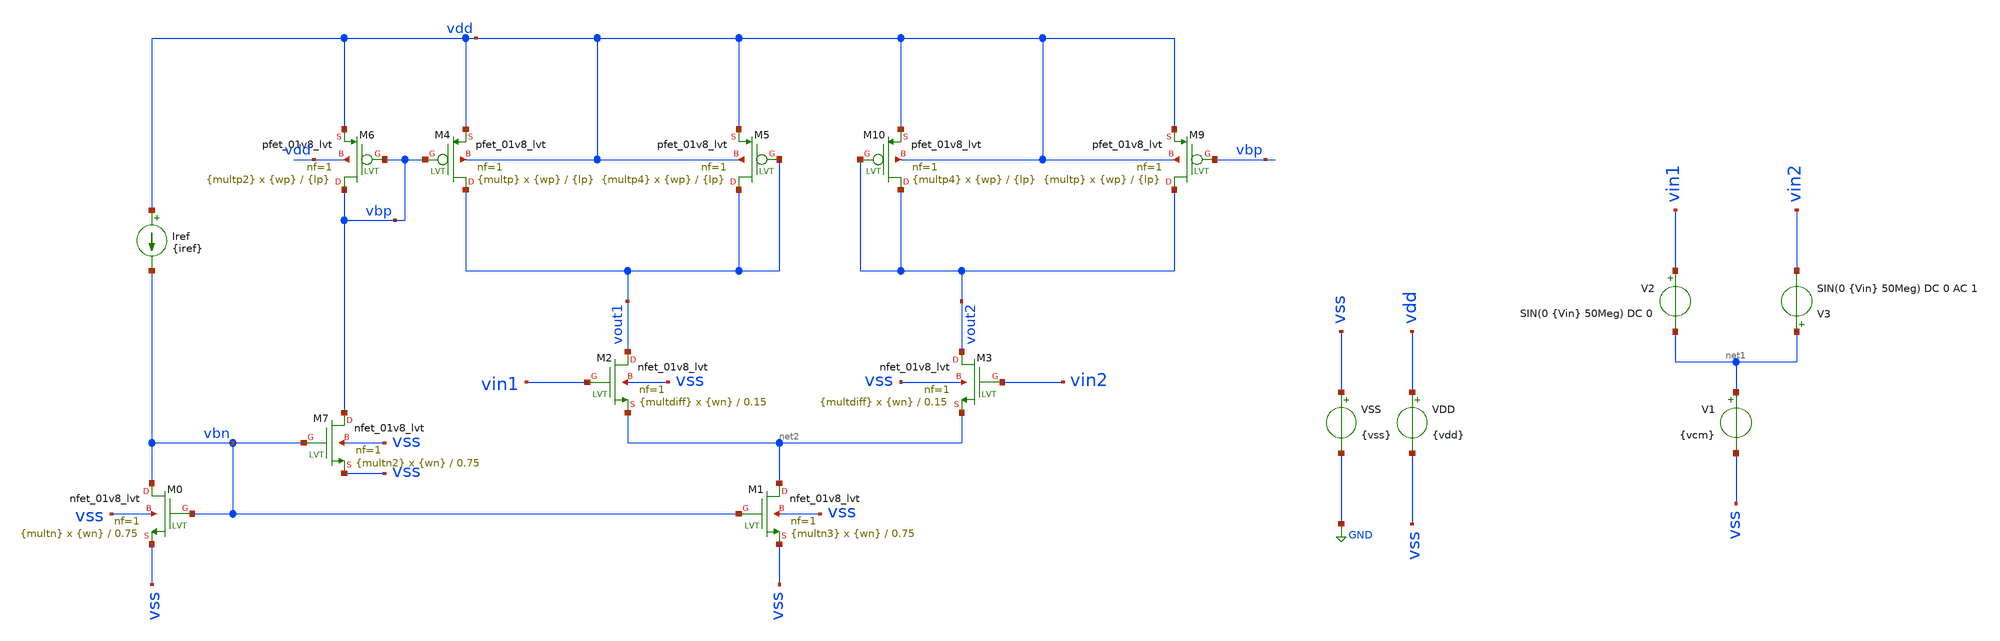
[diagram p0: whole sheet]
** sch_path: tp3/tp3_2.sch
**.subckt tp3_2
Iref vdd vbn {iref}
VSS vss GND {vss}
VDD vdd vss {vdd}
V1 net1 vss {vcm}
XM1 net2 vbn vss vss sky130_fd_pr__nfet_01v8_lvt L=0.75 W={wn} nf=1 ad='int((nf+1)/2) * W/nf * 0.29'
+ as='int((nf+2)/2) * W/nf * 0.29' pd='2*int((nf+1)/2) * (W/nf + 0.29)' ps='2*int((nf+2)/2) * (W/nf + 0.29)'
+ nrd='0.29 / W' nrs='0.29 / W' sa=0 sb=0 sd=0 mult={multn3} m={multn3}
XM0 vbn vbn vss vss sky130_fd_pr__nfet_01v8_lvt L=0.75 W={wn} nf=1 ad='int((nf+1)/2) * W/nf * 0.29' as='int((nf+2)/2) * W/nf * 0.29'
+ pd='2*int((nf+1)/2) * (W/nf + 0.29)' ps='2*int((nf+2)/2) * (W/nf + 0.29)' nrd='0.29 / W' nrs='0.29 / W'
+ sa=0 sb=0 sd=0 mult={multn} m={multn}
XM2 vout1 vin1 net2 vss sky130_fd_pr__nfet_01v8_lvt L=0.15 W={wn} nf=1 ad='int((nf+1)/2) * W/nf * 0.29'
+ as='int((nf+2)/2) * W/nf * 0.29' pd='2*int((nf+1)/2) * (W/nf + 0.29)' ps='2*int((nf+2)/2) * (W/nf + 0.29)'
+ nrd='0.29 / W' nrs='0.29 / W' sa=0 sb=0 sd=0 mult={multdiff} m={multdiff}
XM3 vout2 vin2 net2 vss sky130_fd_pr__nfet_01v8_lvt L=0.15 W={wn} nf=1 ad='int((nf+1)/2) * W/nf * 0.29'
+ as='int((nf+2)/2) * W/nf * 0.29' pd='2*int((nf+1)/2) * (W/nf + 0.29)' ps='2*int((nf+2)/2) * (W/nf + 0.29)'
+ nrd='0.29 / W' nrs='0.29 / W' sa=0 sb=0 sd=0 mult={multdiff} m={multdiff}
V2 vin1 net1 SIN(0 {Vin} 50Meg) DC 0
V3 net1 vin2 SIN(0 {Vin} 50Meg) DC 0 AC 1
XM4 vout1 vbp vdd vdd sky130_fd_pr__pfet_01v8_lvt L={lp} W={wp} nf=1 ad='int((nf+1)/2) * W/nf * 0.29'
+ as='int((nf+2)/2) * W/nf * 0.29' pd='2*int((nf+1)/2) * (W/nf + 0.29)' ps='2*int((nf+2)/2) * (W/nf + 0.29)'
+ nrd='0.29 / W' nrs='0.29 / W' sa=0 sb=0 sd=0 mult={multp} m={multp}
XM6 vbp vbp vdd vdd sky130_fd_pr__pfet_01v8_lvt L={lp} W={wp} nf=1 ad='int((nf+1)/2) * W/nf * 0.29' as='int((nf+2)/2) * W/nf * 0.29'
+ pd='2*int((nf+1)/2) * (W/nf + 0.29)' ps='2*int((nf+2)/2) * (W/nf + 0.29)' nrd='0.29 / W' nrs='0.29 / W'
+ sa=0 sb=0 sd=0 mult={multp2} m={multp2}
XM7 vbp vbn vss vss sky130_fd_pr__nfet_01v8_lvt L=0.75 W={wn} nf=1 ad='int((nf+1)/2) * W/nf * 0.29' as='int((nf+2)/2) * W/nf * 0.29'
+ pd='2*int((nf+1)/2) * (W/nf + 0.29)' ps='2*int((nf+2)/2) * (W/nf + 0.29)' nrd='0.29 / W' nrs='0.29 / W'
+ sa=0 sb=0 sd=0 mult={multn2} m={multn2}
XM5 vout1 vout1 vdd vdd sky130_fd_pr__pfet_01v8_lvt L={lp} W={wp} nf=1 ad='int((nf+1)/2) * W/nf * 0.29'
+ as='int((nf+2)/2) * W/nf * 0.29' pd='2*int((nf+1)/2) * (W/nf + 0.29)' ps='2*int((nf+2)/2) * (W/nf + 0.29)'
+ nrd='0.29 / W' nrs='0.29 / W' sa=0 sb=0 sd=0 mult={multp4} m={multp4}
XM9 vout2 vbp vdd vdd sky130_fd_pr__pfet_01v8_lvt L={lp} W={wp} nf=1 ad='int((nf+1)/2) * W/nf * 0.29'
+ as='int((nf+2)/2) * W/nf * 0.29' pd='2*int((nf+1)/2) * (W/nf + 0.29)' ps='2*int((nf+2)/2) * (W/nf + 0.29)'
+ nrd='0.29 / W' nrs='0.29 / W' sa=0 sb=0 sd=0 mult={multp} m={multp}
XM10 vout2 vout2 vdd vdd sky130_fd_pr__pfet_01v8_lvt L={lp} W={wp} nf=1 ad='int((nf+1)/2) * W/nf * 0.29'
+ as='int((nf+2)/2) * W/nf * 0.29' pd='2*int((nf+1)/2) * (W/nf + 0.29)' ps='2*int((nf+2)/2) * (W/nf + 0.29)'
+ nrd='0.29 / W' nrs='0.29 / W' sa=0 sb=0 sd=0 mult={multp4} m={multp4}
**** begin user architecture code



* Parameters
.param vdd = 1.62
.param vss = 0.0
.param iref = 45u
.param wn = 0.5
.param wp = 1
.param lp = 1
.param multn = 10
.param multn2 = 10
.param multn3 = 21
.param multp = 12
.param multdiff = 4
.param multp2 = 15
.param multp4 = 7
.param Vin = 100m
.param vcm = 1.08

.options TEMP = 125.0

* Models
*.lib ~/skywater/skywater-pdk/libraries/sky130_fd_pr_ngspice/latest/models/corners/sky130.lib TT
*.lib /foss/pdks/sky130A/libs.tech/ngspice/sky130.lib.spice.tt.red tt
.lib /foss/pdks/sky130A/libs.tech/ngspice/sky130.lib.spice ss
* Data to save
.save all  @M.XM0.msky130_fd_pr__nfet_01v8_lvt[id]  @M.XM0.msky130_fd_pr__nfet_01v8_lvt[vds]  @M.XM0.msky130_fd_pr__nfet_01v8_lvt[vgs]  @M.XM0.msky130_fd_pr__nfet_01v8_lvt[vdsat]  @M.XM0.msky130_fd_pr__nfet_01v8_lvt[vth]  @M.XM0.msky130_fd_pr__nfet_01v8_lvt[gm]  @M.XM1.msky130_fd_pr__nfet_01v8_lvt[id]  @M.XM1.msky130_fd_pr__nfet_01v8_lvt[vds]  @M.XM1.msky130_fd_pr__nfet_01v8_lvt[vgs]  @M.XM1.msky130_fd_pr__nfet_01v8_lvt[vdsat]  @M.XM1.msky130_fd_pr__nfet_01v8_lvt[vth]  @M.XM1.msky130_fd_pr__nfet_01v8_lvt[gm]  @M.XM1.msky130_fd_pr__nfet_01v8_lvt[gds]  @M.XM2.msky130_fd_pr__nfet_01v8_lvt[id]  @M.XM2.msky130_fd_pr__nfet_01v8_lvt[vds]  @M.XM2.msky130_fd_pr__nfet_01v8_lvt[vgs]  @M.XM2.msky130_fd_pr__nfet_01v8_lvt[vdsat]  @M.XM2.msky130_fd_pr__nfet_01v8_lvt[vth]  @M.XM2.msky130_fd_pr__nfet_01v8_lvt[gm]  @M.XM2.msky130_fd_pr__nfet_01v8_lvt[gds]  @M.XM3.msky130_fd_pr__nfet_01v8_lvt[id]  @M.XM3.msky130_fd_pr__nfet_01v8_lvt[vds]  @M.XM3.msky130_fd_pr__nfet_01v8_lvt[vgs]  @M.XM3.msky130_fd_pr__nfet_01v8_lvt[vdsat]  @M.XM3.msky130_fd_pr__nfet_01v8_lvt[vth]  @M.XM3.msky130_fd_pr__nfet_01v8_lvt[gm]  @M.XM3.msky130_fd_pr__nfet_01v8_lvt[gds]  @M.XM7.msky130_fd_pr__nfet_01v8_lvt[id]  @M.XM7.msky130_fd_pr__nfet_01v8_lvt[vds]  @M.XM7.msky130_fd_pr__nfet_01v8_lvt[vgs]  @M.XM7.msky130_fd_pr__nfet_01v8_lvt[vdsat]  @M.XM7.msky130_fd_pr__nfet_01v8_lvt[vth]  @M.XM7.msky130_fd_pr__nfet_01v8_lvt[gm]  @M.XM7.msky130_fd_pr__nfet_01v8_lvt[gds]  @M.XM4.msky130_fd_pr__pfet_01v8_lvt[id]  @M.XM4.msky130_fd_pr__pfet_01v8_lvt[vds]  @M.XM4.msky130_fd_pr__pfet_01v8_lvt[vgs]  @M.XM4.msky130_fd_pr__pfet_01v8_lvt[vdsat]  @M.XM4.msky130_fd_pr__pfet_01v8_lvt[vth]  @M.XM4.msky130_fd_pr__pfet_01v8_lvt[gm]  @M.XM4.msky130_fd_pr__pfet_01v8_lvt[gds]  @M.XM5.msky130_fd_pr__pfet_01v8_lvt[id]  @M.XM5.msky130_fd_pr__pfet_01v8_lvt[vds]  @M.XM5.msky130_fd_pr__pfet_01v8_lvt[vgs]  @M.XM5.msky130_fd_pr__pfet_01v8_lvt[vdsat]  @M.XM5.msky130_fd_pr__pfet_01v8_lvt[vth]  @M.XM5.msky130_fd_pr__pfet_01v8_lvt[gm]  @M.XM5.msky130_fd_pr__pfet_01v8_lvt[gds]  @M.XM6.msky130_fd_pr__pfet_01v8_lvt[id]  @M.XM6.msky130_fd_pr__pfet_01v8_lvt[vds]  @M.XM6.msky130_fd_pr__pfet_01v8_lvt[vgs]  @M.XM6.msky130_fd_pr__pfet_01v8_lvt[vdsat]  @M.XM6.msky130_fd_pr__pfet_01v8_lvt[vth]  @M.XM6.msky130_fd_pr__pfet_01v8_lvt[gm]  @M.XM6.msky130_fd_pr__pfet_01v8_lvt[gds]  @M.XM9.msky130_fd_pr__pfet_01v8_lvt[id]  @M.XM9.msky130_fd_pr__pfet_01v8_lvt[vds]  @M.XM9.msky130_fd_pr__pfet_01v8_lvt[vgs]  @M.XM9.msky130_fd_pr__pfet_01v8_lvt[vdsat]  @M.XM9.msky130_fd_pr__pfet_01v8_lvt[vth]  @M.XM9.msky130_fd_pr__pfet_01v8_lvt[gm]  @M.XM9.msky130_fd_pr__pfet_01v8_lvt[gds]  @M.XM10.msky130_fd_pr__pfet_01v8_lvt[id]  @M.XM10.msky130_fd_pr__pfet_01v8_lvt[vds]  @M.XM10.msky130_fd_pr__pfet_01v8_lvt[vgs]  @M.XM10.msky130_fd_pr__pfet_01v8_lvt[vdsat]  @M.XM10.msky130_fd_pr__pfet_01v8_lvt[vth]  @M.XM10.msky130_fd_pr__pfet_01v8_lvt[gm]  @M.XM10.msky130_fd_pr__pfet_01v8_lvt[gds]




* Simulation
.control

  ac dec 100 10k 100G
  let vdiff = vout1-vout2
  let vindiff = vin1-vin2
  setplot ac1
  meas ac GBW when vdb(vdiff) = 0
  meas ac DCG find vdb(vdiff) at=10k
  meas ac PM find vp(vdiff) when vdb(vdiff)=0
  print PM*180/PI
  meas ac GM find vdb(vdiff) when vp(vdiff)=0
  plot vdb(vdiff) {vp(vdiff)*180/PI}
  write tp3_2_ac.raw

  reset
  tran 0.01n 100n
  let vdiff = vout1-vout2
  let vindiff = vin1-vin2
  plot v(vindiff) v(vdiff)
 plot v(vout1) v(vout2)
  write tp3_2_tran.raw

  reset
  op
  save all
  print all
  unset filetype
  write tp3_2.raw


.endc

.end


**** end user architecture code
**.ends
.GLOBAL GND
.end
